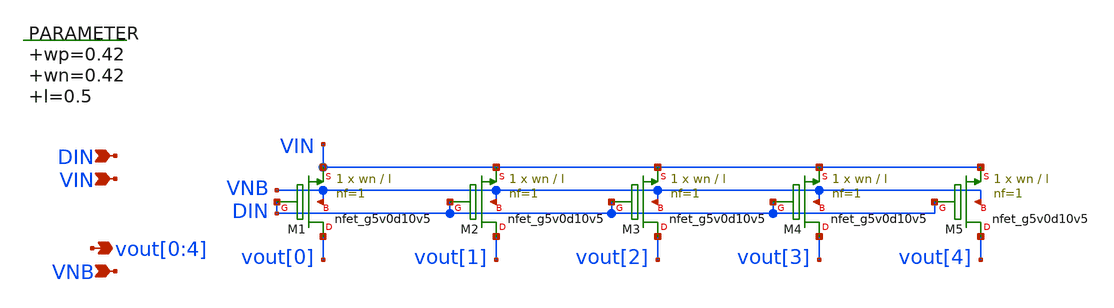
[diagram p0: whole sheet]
** sch_path: xschem/seg_selector_1.sch
**.subckt seg_selector_1 vout[0],vout[1],vout[2],vout[3],vout[4] VNB DIN VIN
*.opin vout[0],vout[1],vout[2],vout[3],vout[4]
*.ipin VNB
*.ipin DIN
*.ipin VIN
.param wp=0.42 wn=0.42 l=0.5

XM1 vout[0] DIN VIN VNB sky130_fd_pr__nfet_g5v0d10v5 L=l W=wn nf=1 ad='int((nf+1)/2) * W/nf * 0.29' as='int((nf+2)/2) * W/nf * 0.29'
+ pd='2*int((nf+1)/2) * (W/nf + 0.29)' ps='2*int((nf+2)/2) * (W/nf + 0.29)' nrd='0.29 / W' nrs='0.29 / W'
+ sa=0 sb=0 sd=0 mult=1 m=1
XM2 vout[1] DIN VIN VNB sky130_fd_pr__nfet_g5v0d10v5 L=l W=wn nf=1 ad='int((nf+1)/2) * W/nf * 0.29' as='int((nf+2)/2) * W/nf * 0.29'
+ pd='2*int((nf+1)/2) * (W/nf + 0.29)' ps='2*int((nf+2)/2) * (W/nf + 0.29)' nrd='0.29 / W' nrs='0.29 / W'
+ sa=0 sb=0 sd=0 mult=1 m=1
XM3 vout[2] DIN VIN VNB sky130_fd_pr__nfet_g5v0d10v5 L=l W=wn nf=1 ad='int((nf+1)/2) * W/nf * 0.29' as='int((nf+2)/2) * W/nf * 0.29'
+ pd='2*int((nf+1)/2) * (W/nf + 0.29)' ps='2*int((nf+2)/2) * (W/nf + 0.29)' nrd='0.29 / W' nrs='0.29 / W'
+ sa=0 sb=0 sd=0 mult=1 m=1
XM4 vout[3] DIN VIN VNB sky130_fd_pr__nfet_g5v0d10v5 L=l W=wn nf=1 ad='int((nf+1)/2) * W/nf * 0.29' as='int((nf+2)/2) * W/nf * 0.29'
+ pd='2*int((nf+1)/2) * (W/nf + 0.29)' ps='2*int((nf+2)/2) * (W/nf + 0.29)' nrd='0.29 / W' nrs='0.29 / W'
+ sa=0 sb=0 sd=0 mult=1 m=1
XM5 vout[4] DIN VIN VNB sky130_fd_pr__nfet_g5v0d10v5 L=l W=wn nf=1 ad='int((nf+1)/2) * W/nf * 0.29' as='int((nf+2)/2) * W/nf * 0.29'
+ pd='2*int((nf+1)/2) * (W/nf + 0.29)' ps='2*int((nf+2)/2) * (W/nf + 0.29)' nrd='0.29 / W' nrs='0.29 / W'
+ sa=0 sb=0 sd=0 mult=1 m=1
**.ends
.end
